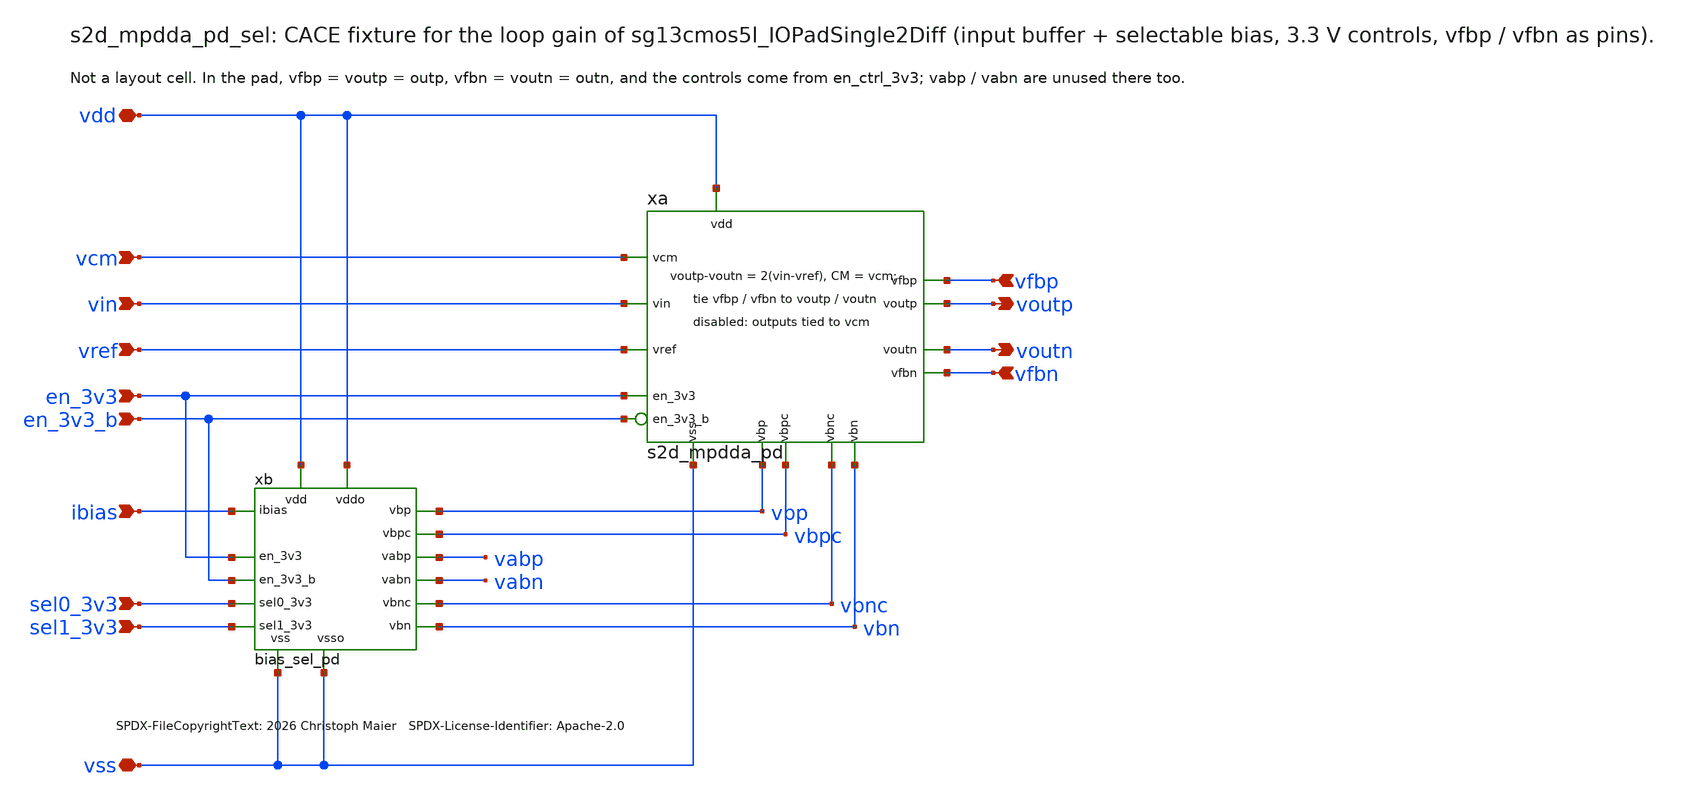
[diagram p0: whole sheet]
** sch_path: sudelbuecher/design_considerations/consolidation/ab_regroup_2026-10-28/before/macros/sg13cmos5l_IOPadSingle2Diff/schematic/xschem/s2d_mpdda_pd_sel.sch
* SPDX-FileCopyrightText: 2026 Christoph Maier SPDX-License-Identifier: Apache-2.0
**.subckt s2d_mpdda_pd_sel vdd vin vref vcm en_3v3 en_3v3_b ibias sel0_3v3 sel1_3v3 vss voutp voutn
*+ vfbp vfbn
*.iopin vdd
*.ipin vin
*.ipin vref
*.ipin vcm
*.ipin en_3v3
*.ipin en_3v3_b
*.ipin ibias
*.ipin sel0_3v3
*.ipin sel1_3v3
*.iopin vss
*.opin voutp
*.opin voutn
*.ipin vfbp
*.ipin vfbn
xb vdd vss vdd vss ibias vbp vbn vbpc vbnc vabp vabn en_3v3 sel0_3v3 sel1_3v3 en_3v3_b bias_sel_pd
xa vdd vss vin vref vcm voutp voutn vfbp vfbn vbp vbn vbpc vbnc en_3v3 en_3v3_b s2d_mpdda_pd
**.ends
.end
